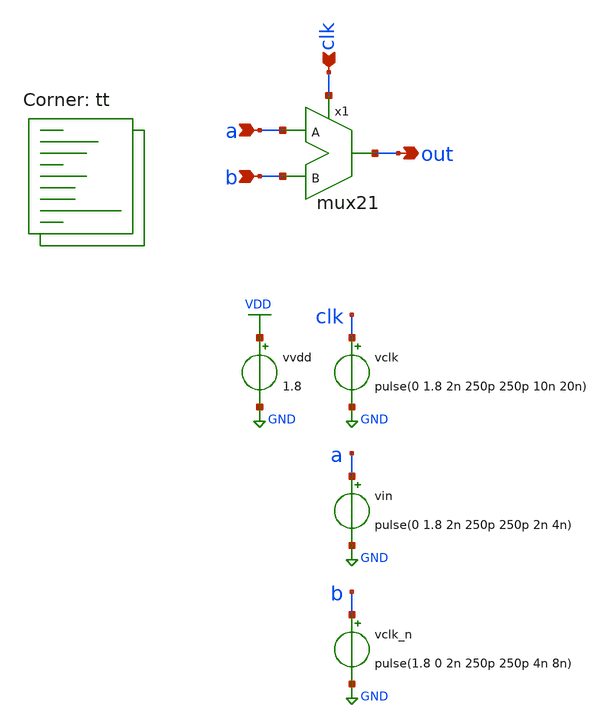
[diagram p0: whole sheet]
** sch_path: xschem/sim/tb_mux21.sch
**.subckt tb_mux21 out a clk b
*.opin out
*.ipin a
*.ipin clk
*.ipin b
vvdd VDD GND 1.8
vclk clk GND pulse(0 1.8 2n 250p 250p 10n 20n)
vin a GND pulse(0 1.8 2n 250p 250p 2n 4n)
vclk_n b GND pulse(1.8 0 2n 250p 250p 4n 8n)
x1 clk a out b mux21
**** begin user architecture code
.lib $::SKYWATER_MODELS/sky130.lib.spice tt


.control
* Transient analysis
TRAN 1p 40n
save all
set filetype=binary
write tb_mux21_tran.raw
.endc


**** end user architecture code
**.ends

* expanding   symbol:  mux21.sym # of pins=4
** sym_path: xschem/mux21.sym
** sch_path: xschem/mux21.sch
.subckt mux21 S A Y B
*.ipin S
*.ipin A
*.ipin B
*.opin Y
x1 S A Y net1 t_gate
x2 net1 B Y S t_gate
x3 net1 S inv
.ends


* expanding   symbol:  t_gate.sym # of pins=4
** sym_path: xschem/t_gate.sym
** sch_path: xschem/t_gate.sch
.subckt t_gate E_n in out E
*.ipin in
*.opin out
*.ipin E
*.ipin E_n
XM1 in E out GND sky130_fd_pr__nfet_01v8 L=0.15 W=0.42 nf=1 ad='int((nf+1)/2) * W/nf * 0.29' as='int((nf+2)/2) * W/nf * 0.29'
+ pd='2*int((nf+1)/2) * (W/nf + 0.29)' ps='2*int((nf+2)/2) * (W/nf + 0.29)' nrd='0.29 / W' nrs='0.29 / W'
+ sa=0 sb=0 sd=0 mult=1 m=1
XM2 in E_n out VDD sky130_fd_pr__pfet_01v8 L=0.15 W=0.84 nf=1 ad='int((nf+1)/2) * W/nf * 0.29' as='int((nf+2)/2) * W/nf * 0.29'
+ pd='2*int((nf+1)/2) * (W/nf + 0.29)' ps='2*int((nf+2)/2) * (W/nf + 0.29)' nrd='0.29 / W' nrs='0.29 / W'
+ sa=0 sb=0 sd=0 mult=1 m=1
.ends


* expanding   symbol:  inv.sym # of pins=2
** sym_path: xschem/inv.sym
** sch_path: xschem/inv.sch
.subckt inv Z A
*.ipin a
*.opin z
XM1 z a GND GND sky130_fd_pr__nfet_01v8 L=0.15 W=0.42 nf=1 ad='int((nf+1)/2) * W/nf * 0.29' as='int((nf+2)/2) * W/nf * 0.29'
+ pd='2*int((nf+1)/2) * (W/nf + 0.29)' ps='2*int((nf+2)/2) * (W/nf + 0.29)' nrd='0.29 / W' nrs='0.29 / W'
+ sa=0 sb=0 sd=0 mult=1 m=1
XM2 z a VDD VDD sky130_fd_pr__pfet_01v8 L=0.15 W=0.84 nf=1 ad='int((nf+1)/2) * W/nf * 0.29' as='int((nf+2)/2) * W/nf * 0.29'
+ pd='2*int((nf+1)/2) * (W/nf + 0.29)' ps='2*int((nf+2)/2) * (W/nf + 0.29)' nrd='0.29 / W' nrs='0.29 / W'
+ sa=0 sb=0 sd=0 mult=1 m=1
.ends

.GLOBAL VDD
.GLOBAL GND
.end
